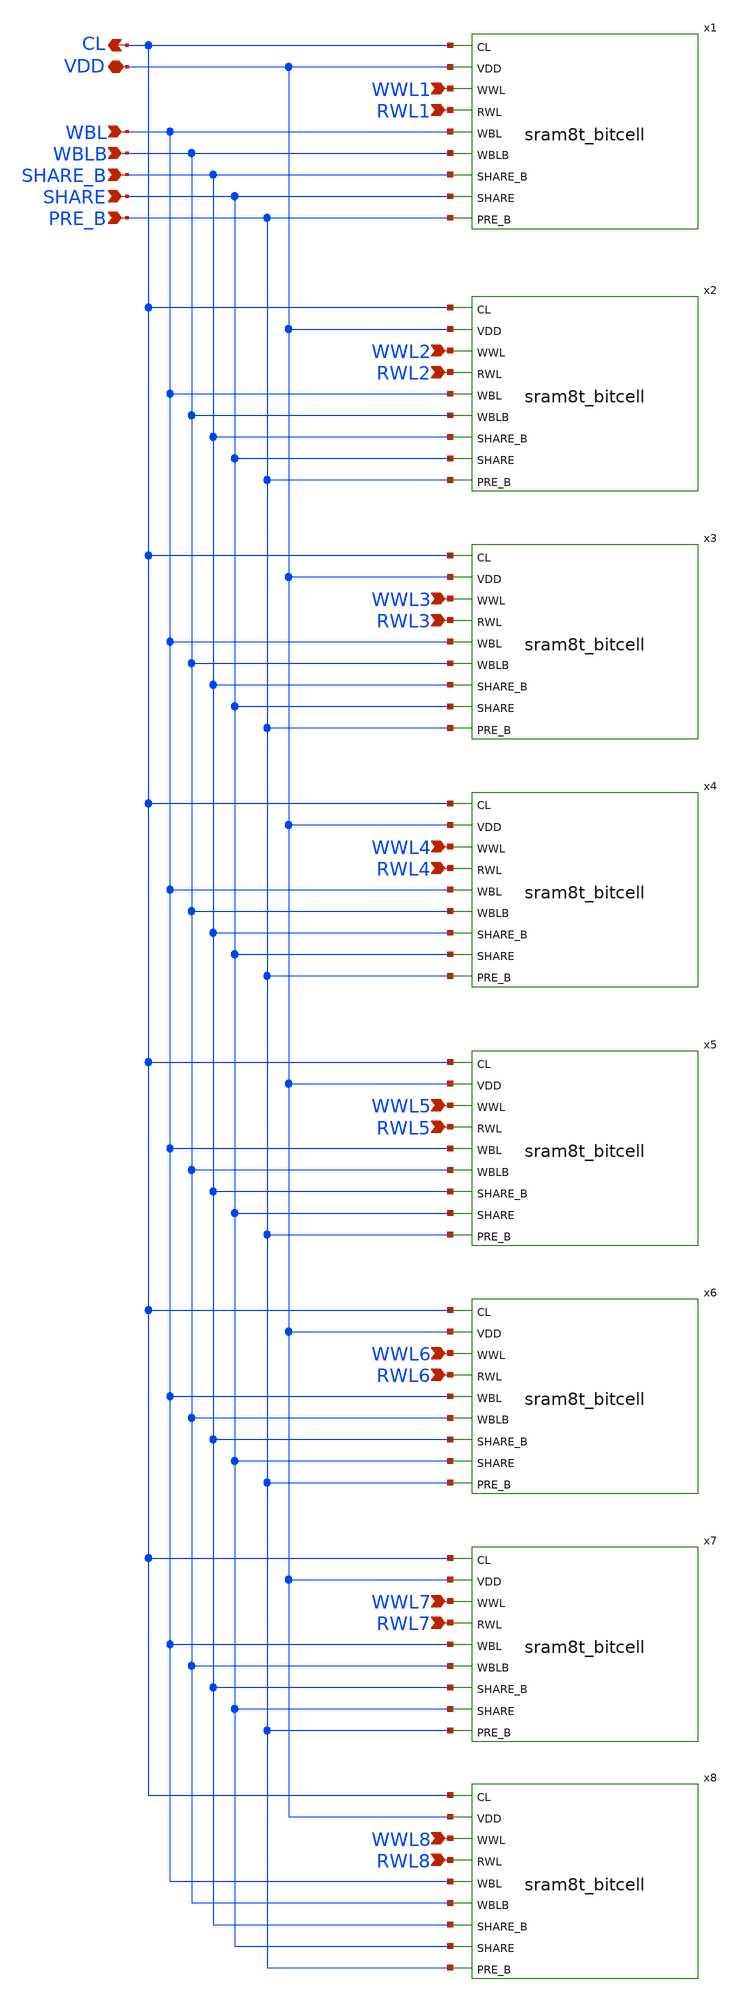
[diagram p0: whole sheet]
** sch_path: schematics/column8t.sch
**.subckt column8t VDD WBL WBLB SHARE_B SHARE PRE_B CL WWL1 RWL1 WWL2 RWL2 WWL3 RWL3 WWL4 RWL4 WWL5
*+ RWL5 WWL6 RWL6 WWL7 RWL7 WWL8 RWL8
*.iopin VDD
*.ipin WBL
*.ipin WBLB
*.ipin SHARE_B
*.ipin SHARE
*.ipin PRE_B
*.opin CL
*.ipin WWL1
*.ipin RWL1
*.ipin WWL2
*.ipin RWL2
*.ipin WWL3
*.ipin RWL3
*.ipin WWL4
*.ipin RWL4
*.ipin WWL5
*.ipin RWL5
*.ipin WWL6
*.ipin RWL6
*.ipin WWL7
*.ipin RWL7
*.ipin WWL8
*.ipin RWL8
x1 CL VDD WWL1 RWL1 WBL WBLB SHARE_B SHARE PRE_B sram8t_bitcell
x2 CL VDD WWL2 RWL2 WBL WBLB SHARE_B SHARE PRE_B sram8t_bitcell
x3 CL VDD WWL3 RWL3 WBL WBLB SHARE_B SHARE PRE_B sram8t_bitcell
x4 CL VDD WWL4 RWL4 WBL WBLB SHARE_B SHARE PRE_B sram8t_bitcell
x5 CL VDD WWL5 RWL5 WBL WBLB SHARE_B SHARE PRE_B sram8t_bitcell
x6 CL VDD WWL6 RWL6 WBL WBLB SHARE_B SHARE PRE_B sram8t_bitcell
x7 CL VDD WWL7 RWL7 WBL WBLB SHARE_B SHARE PRE_B sram8t_bitcell
x8 CL VDD WWL8 RWL8 WBL WBLB SHARE_B SHARE PRE_B sram8t_bitcell
**.ends
.end
